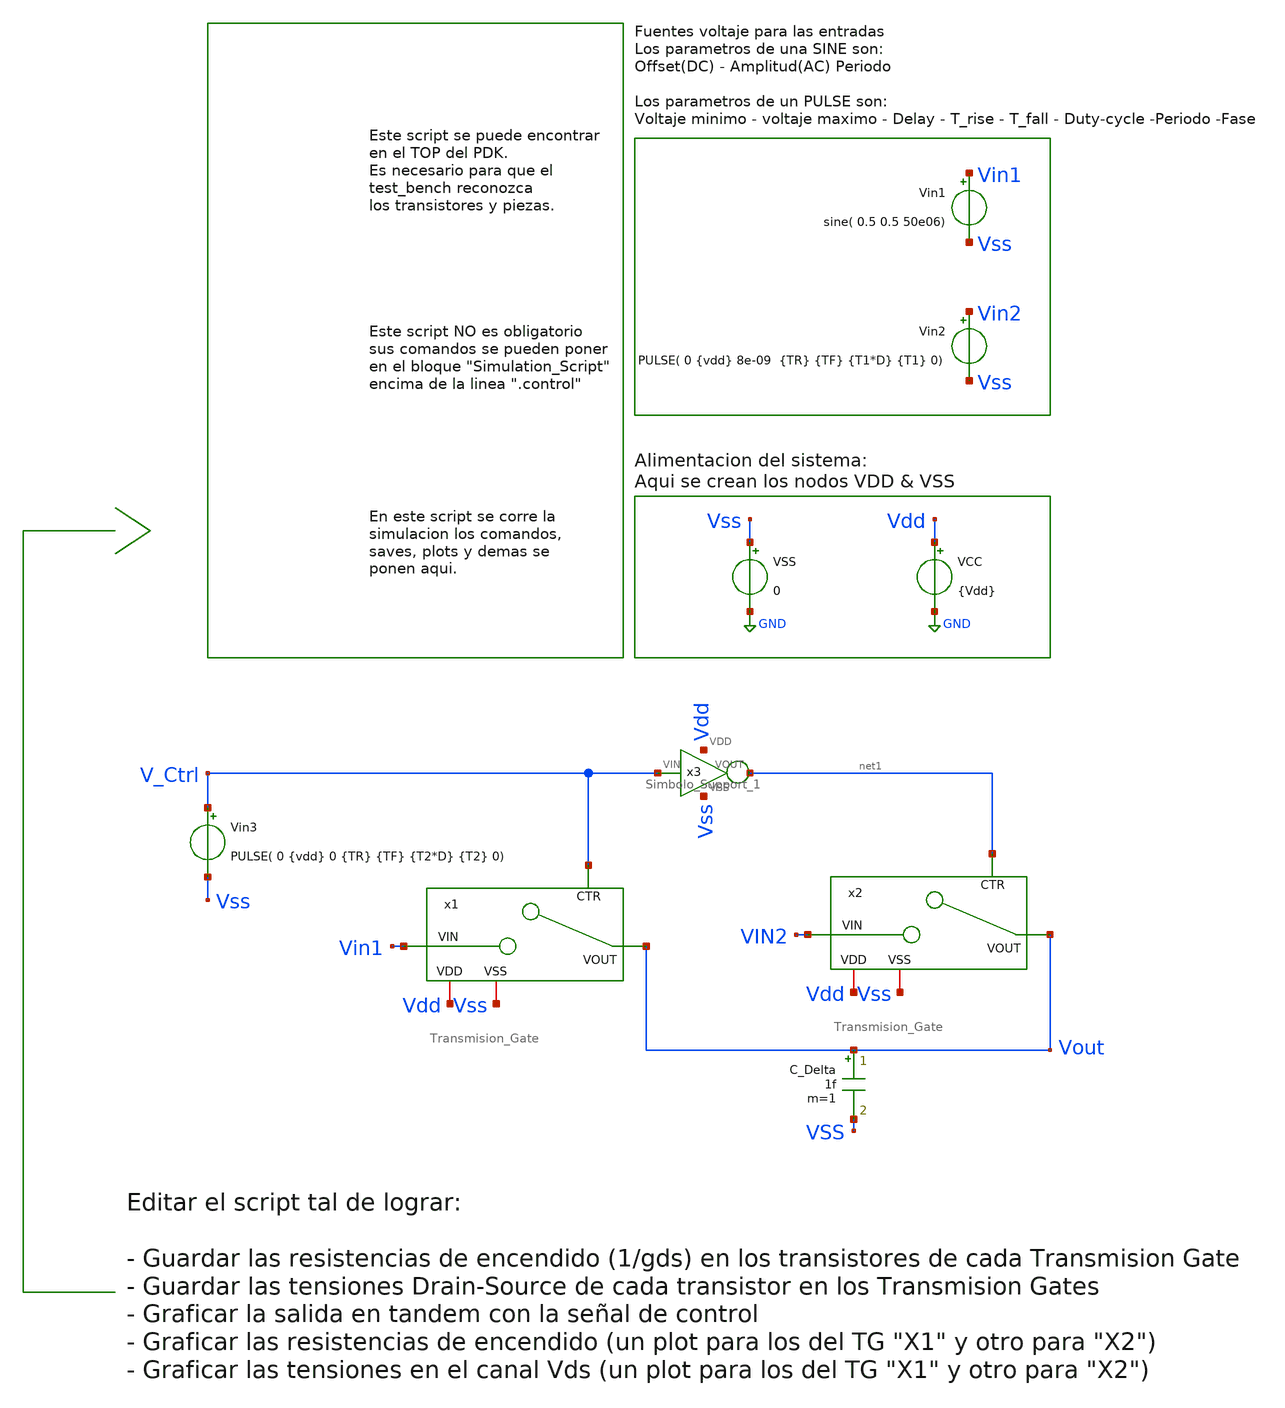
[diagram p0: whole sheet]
** sch_path: Taller2_extendido/Insumos/Transmision_Gate_Test.sch
**.subckt Transmision_Gate_Test
VCC Vdd GND {Vdd}
VSS Vss GND 0
Vin1 Vin1 Vss sine( 0.5 0.5 50e06)
Vin2 Vin2 Vss PULSE( 0 {vdd} 8e-09 {TR} {TF} {T1*D} {T1} 0)
C_Delta Vout VSS 1f m=1
Vin3 V_Ctrl Vss PULSE( 0 {vdd} 0 {TR} {TF} {T2*D} {T2} 0)
x3 Vdd V_Ctrl net1 Vss Simbolo_Support_1
x2 Vout VIN2 Vdd net1 Vss Transmision_Gate
x1 Vout Vin1 Vdd V_Ctrl Vss Transmision_Gate
**** begin user architecture code


.param corner=0

.if (corner==0)
.lib $::SG13G2_MODELS/cornerMOSlv.lib mos_tt
.lib $::SG13G2_MODELS/cornerMOSlv.lib mos_tt
.lib $::SG13G2_MODELS/cornerRES.lib res_typ
.lib $::SG13G2_MODELS/cornerCAP.lib cap_typ
.endif



.param Vdd = 1.2

.param temp = 27
.param TR = 240e-12
.param TF = 240e-12
.param D = 0.5
.param T2 = 200e-09
.param T1 = 15e-09





.save all

*.OPTION CSHUNT=0.05e-12
.OPTION ABSTOL=1e-15.
*.OPTION GMIN=1.0e-12.
.OPTION ITL1=1e5
*.OPTION RSHUNT=1e12
.OPTION RELTOL=1e-5
.

*Guardar transconductancias de compuerta Source-Drain

*Gruardar la tension Drain-source de los Mosfet en el Switch/Transmision-gate

.control

tran 0.1n  400n

*Convertir en variables transientes (poniendolas post sim tran) de variables guardadas


*Guardar las resistencias de encendido se guarda como variable 1/gds:



*PLOTS

*Graficar salida en comparacion con la señal de control

*Graficar resistencias de encendido en cada transistor de los TG

*Graficar las diferencias de tension entre Drain y Source en cada MOS de los TG

.endc




**** end user architecture code
**.ends

* expanding   symbol:  Simbolo_Support_1.sym # of pins=4
** sym_path: Taller2_extendido/Insumos/Simbolo_Support_1.sym
** sch_path: Taller2_extendido/Insumos/Simbolo_Support_1.sch
.subckt Simbolo_Support_1 VDD VIN VOUT VSS
*.ipin VIN
*.iopin VDD
*.iopin VSS
*.opin VOUT
XM1 VOUT VIN VDD VDD sg13_lv_pmos w=1.0u l=0.15u ng=1 m=1 mm_ok=1
XM2 VOUT VIN VSS VSS sg13_lv_nmos w=1.0u l=0.15u ng=1 m=1 mm_ok=1
.ends


* expanding   symbol:  Transmision_Gate.sym # of pins=5
** sym_path: Taller2_extendido/Insumos/Transmision_Gate.sym
** sch_path: Taller2_extendido/Insumos/Transmision_Gate.sch
.subckt Transmision_Gate VOUT VIN VDD CTR VSS
*.ipin VIN
*.iopin VDD
*.iopin VSS
*.ipin CTR
*.opin VOUT
XM1 VOUT net1 VIN VDD sg13_lv_pmos w=6.0u l=0.15u ng=1 m=1 mm_ok=1
XM2 VOUT CTR VIN VSS sg13_lv_nmos w=2.0u l=0.15u ng=1 m=1 mm_ok=1
x1 VDD CTR net1 VSS Simbolo_Support_1
.ends

.GLOBAL GND
.end
